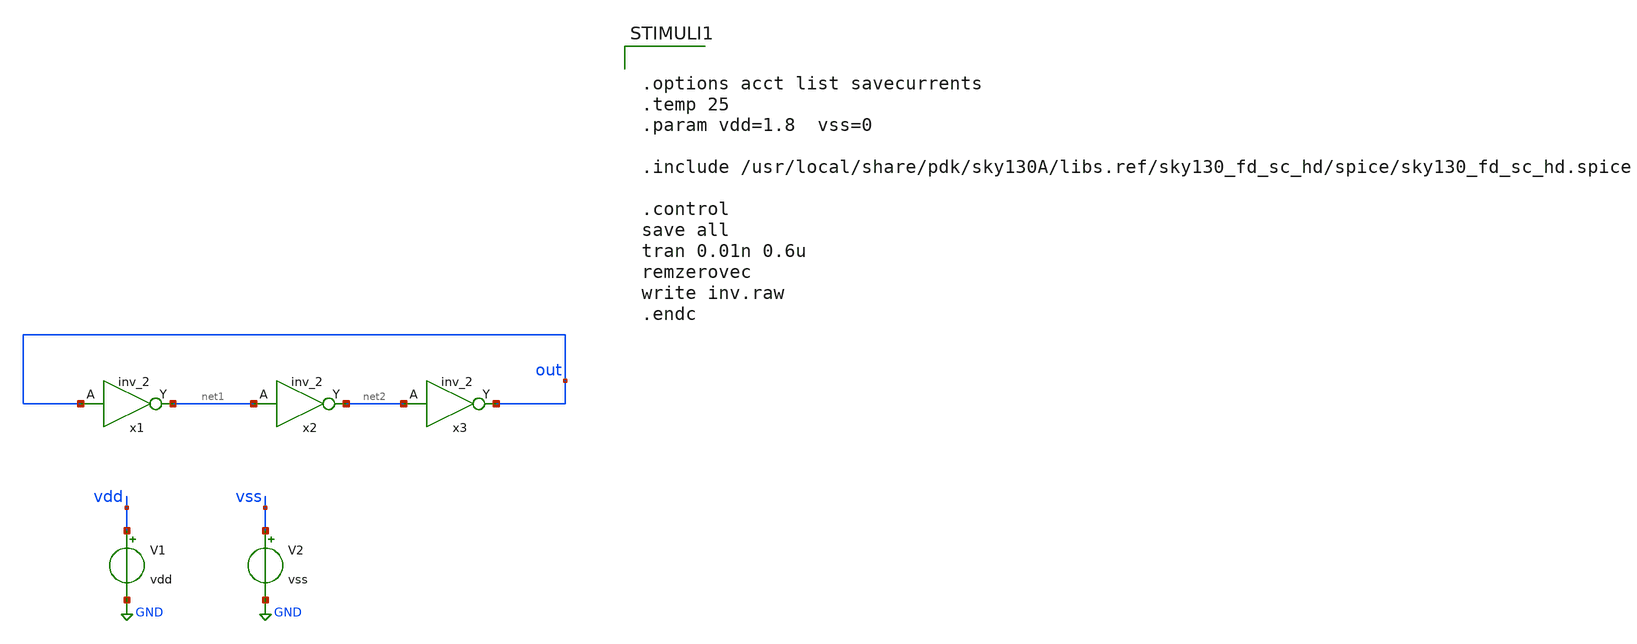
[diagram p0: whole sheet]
** sch_path: xschem01/inv.sch
**.subckt inv
x1 out VSS VSS VDD VDD net1 sky130_fd_sc_hd__inv_2
x2 net1 VSS VSS VDD VDD net2 sky130_fd_sc_hd__inv_2
x3 net2 VSS VSS VDD VDD out sky130_fd_sc_hd__inv_2
V1 vdd GND vdd
V2 vss GND vss
**** begin user architecture code

** opencircuitdesign pdks install
.lib $::SKYWATER_MODELS/sky130.lib.spice tt




.options acct list savecurrents
.temp 25
.param vdd=1.8  vss=0

.include /usr/local/share/pdk/sky130A/libs.ref/sky130_fd_sc_hd/spice/sky130_fd_sc_hd.spice

.control
save all
tran 0.01n 0.6u
remzerovec
write inv.raw
.endc


**** end user architecture code
**.ends
.GLOBAL GND
.end
